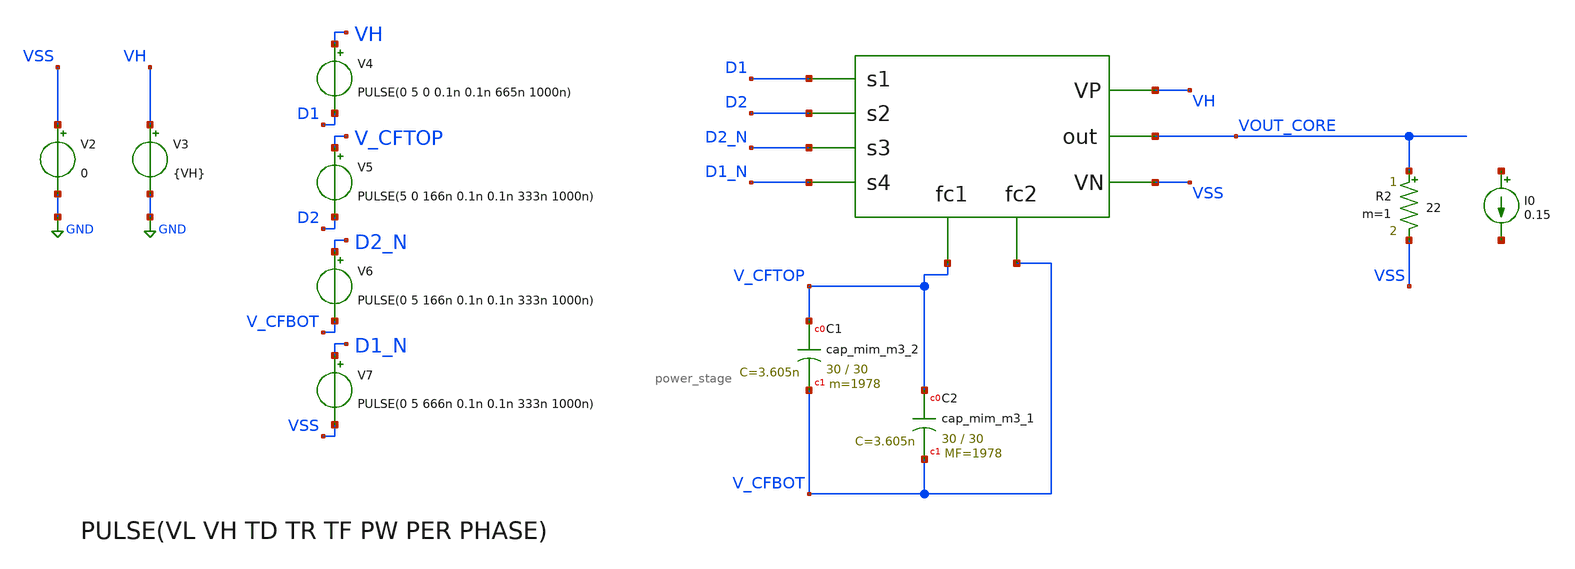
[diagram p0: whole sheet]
** sch_path: xschem/hierarchy_sch/DCDC_5V_FINAL/DCDC_v1p5_1MHz_NMOS_PMOS_sng.sch
**.subckt DCDC_v1p5_1MHz_NMOS_PMOS_sng
V4 VH D1 PULSE(0 5 0 0.1n 0.1n 665n 1000n)
V2 VSS GND 0
V6 D2_N V_CFBOT PULSE(0 5 166n 0.1n 0.1n 333n 1000n)
V3 VH GND {VH}
V5 V_CFTOP D2 PULSE(5 0 166n 0.1n 0.1n 333n 1000n)
V7 D1_N VSS PULSE(0 5 666n 0.1n 0.1n 333n 1000n)
X1 D1 D2 D2_N D1_N V_CFTOP V_CFBOT VOUT_CORE VH VSS power_stage
I0 net1 net2 0.15
R2 VOUT_CORE VSS 22 m=1
XC1 V_CFTOP V_CFBOT sky130_fd_pr__cap_mim_m3_2 W=30 L=30 MF=1978 m=1978
XC2 V_CFTOP V_CFBOT sky130_fd_pr__cap_mim_m3_1 W=30 L=30 MF=1978 m=1978
**** begin user architecture code


.param VIN = 5
.param VH = 5
.param RL = 50
.option scale=1e-6
*.option temp=70
.ic v(V_CFTOP) = VH/2
.ic v(vout_core)=0
.ic v(V_CFBOT) = 0
*.probe vd(MP2:G:S)
*.save all
*.save v(d1) v(d2) v(d1top_5v) v(d2_5v) v(d2bot_5v) v(d1bot_5v) v(vout) v(vout_core) v(vdd) v(vh) i(v1) i(v5) i(vmeas) v(v_cftop,v_cfbot)
.save v(D1) v(D2) v(D1_N) v(D2_N) v(VOUT_CORE) v(vh) i(v3) v(v_cftop,v_cfbot) v(D1,v_cftop) v(D2,vout_core) v(D2_N,v_cfbot) v(D1_Nv,VSS)
.save @m.xm4.msky130_fd_pr__nfet_g5v0d10v5[vds]
.param mc_mm_switch=0
*.lib /home/jorge/Documents/Postdoc/share/pdk/sky130A/libs.tech/ngspice/sky130.lib.spice tt
*.lib /usr/share/pdk/sky130A/libs.tech/ngspice/sky130.lib.spice ss
.lib /foss/pdk/sky130A/libs.tech/ngspice/sky130.lib.spice TT
*.include /usr/share/pdk/sky130A/libs.ref/sky130_fd_sc_hvl/spice/sky130_fd_sc_hvl.spice
*.include /home/jorge/Documents/Postdoc/share/pdk/sky130A/libs.ref/sky130_fd_sc_hvl/spice/sky130_fd_sc_hvl.spice
.options savecurrents
.control
*save all
tran 100n 3u
write DCDC_v1p4_5MHz_NMOS_PMOS.raw
*wrdata
*+ ~/Documents/Postdoc/chipathon2022/3LFCC_AC3E/xschem/dev_switches/DCDC_5V_FINAL/3LFCC_v1p4.txt tran.v(vout) tran.i(vmeas) tran.v(vdd) tran.i(v3) tran.v(vh) tran.i(v5)
wrdata /foss/designs/personal/3LFCC_AC3E/xschem/hierarchy_sch/DCDC_5V_FINAL/3LFCC_v1p4.txt
+ tran.v(vout_core) tran.i(v1)

*plot v(d1top_5v) v(d2_5v)
*plot v(d2bot_5v) v(d1bot_5v)
plot v(v_cftop,v_cfbot) v(vout_core)
*plot v(D1,VH) v(D1_N,VSS)
*plot v(D2,V_CFTOP) v(D2_N,V_CFBOT)
*plot  v(vout_core)
plot i(v3) v(D1,VH) v(D1_N,VSS)
plot i(v3) v(D2,V_CFTOP) v(D2_N,V_CFBOT)
*plot i(v1)
plot i(v3) v(v_cftop,v_cfbot) v(D1,VH) v(D1_N,VSS)  v(D2,V_CFTOP) v(D2_N,V_CFBOT)
plot @m.xm4.msky130_fd_pr__nfet_g5v0d10v5[vds]


*plot v(d1top_5v) v(d2_5v) v(d2bot_5v) v(d1bot_5v) v(v_cftop,v_cfbot) v(vout)
*plot v(v_cftop,v_cfbot) v(vout)
.endc


**** end user architecture code
**.ends

* expanding   symbol:  personal/3LFCC_AC3E/xschem/hierarchy_sch/power_stage.sym # of pins=9
** sym_path: xschem/hierarchy_sch/power_stage.sym
** sch_path: xschem/hierarchy_sch/power_stage.sch
.subckt power_stage s1 s2 s3 s4 fc1 fc2 out VP VN
*.ipin s1
*.ipin s2
*.ipin s3
*.ipin s4
*.iopin VP
*.iopin VN
*.opin out
*.opin fc1
*.opin fc2
X1 s2 fc1 s1 VP out transistor_group_one
X2 s4 fc2 s3 out VN transistor_group_two
.ends


* expanding   symbol:  personal/3LFCC_AC3E/xschem/hierarchy_sch/transistor_group_one.sym # of pins=5
** sym_path: xschem/hierarchy_sch/transistor_group_one.sym
** sch_path: xschem/hierarchy_sch/transistor_group_one.sch
.subckt transistor_group_one s2 fc1 s1 VP out
*.iopin VP
*.ipin s1
*.ipin s2
*.opin fc1
*.iopin out
XM3 out s2 fc1 fc1 sky130_fd_pr__pfet_g5v0d10v5 L=0.5 W=4.38 nf=1 ad='int((nf+1)/2) * W/nf * 0.29' as='int((nf+2)/2) * W/nf * 0.29'
+ pd='2*int((nf+1)/2) * (W/nf + 0.29)' ps='2*int((nf+2)/2) * (W/nf + 0.29)' nrd='0.29 / W' nrs='0.29 / W'
+ sa=0 sb=0 sd=0 mult=4506 m=4506
XM4 fc1 s1 VP VP sky130_fd_pr__pfet_g5v0d10v5 L=0.5 W=4.38 nf=1 ad='int((nf+1)/2) * W/nf * 0.29' as='int((nf+2)/2) * W/nf * 0.29'
+ pd='2*int((nf+1)/2) * (W/nf + 0.29)' ps='2*int((nf+2)/2) * (W/nf + 0.29)' nrd='0.29 / W' nrs='0.29 / W'
+ sa=0 sb=0 sd=0 mult=4506 m=4506
.ends


* expanding   symbol:  personal/3LFCC_AC3E/xschem/hierarchy_sch/transistor_group_two.sym # of pins=5
** sym_path: xschem/hierarchy_sch/transistor_group_two.sym
** sch_path: xschem/hierarchy_sch/transistor_group_two.sch
.subckt transistor_group_two s4 fc2 s3 out VN
*.iopin out
*.ipin s3
*.ipin s4
*.opin fc2
*.iopin VN
XM1 out s3 fc2 fc2 sky130_fd_pr__nfet_g5v0d10v5 L=0.5 W=4.38 nf=1 ad='int((nf+1)/2) * W/nf * 0.29' as='int((nf+2)/2) * W/nf * 0.29'
+ pd='2*int((nf+1)/2) * (W/nf + 0.29)' ps='2*int((nf+2)/2) * (W/nf + 0.29)' nrd='0.29 / W' nrs='0.29 / W'
+ sa=0 sb=0 sd=0 mult=2520 m=2520
XM2 fc2 s4 VN VN sky130_fd_pr__nfet_g5v0d10v5 L=0.5 W=4.38 nf=1 ad='int((nf+1)/2) * W/nf * 0.29' as='int((nf+2)/2) * W/nf * 0.29'
+ pd='2*int((nf+1)/2) * (W/nf + 0.29)' ps='2*int((nf+2)/2) * (W/nf + 0.29)' nrd='0.29 / W' nrs='0.29 / W'
+ sa=0 sb=0 sd=0 mult=2520 m=2520
.ends

.GLOBAL GND
.end
